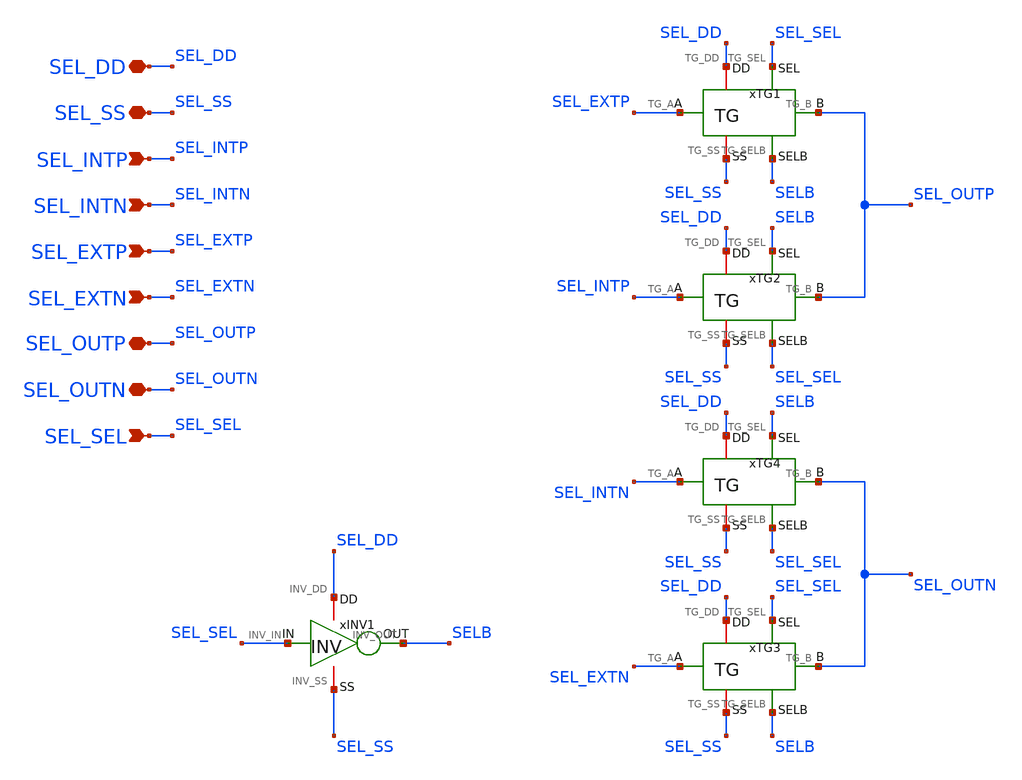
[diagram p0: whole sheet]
** sch_path: Design_Files/IC Design/Schematic/AFE_BLOCKS/SEL/SEL.sch
**.subckt SEL SEL_DD SEL_SS SEL_INTP SEL_INTN SEL_OUTP SEL_OUTN SEL_EXTP SEL_EXTN SEL_SEL
*.iopin SEL_DD
*.iopin SEL_SS
*.ipin SEL_INTP
*.ipin SEL_INTN
*.iopin SEL_OUTP
*.iopin SEL_OUTN
*.ipin SEL_EXTP
*.ipin SEL_EXTN
*.ipin SEL_SEL
xINV1 SEL_DD SEL_SS SEL_SEL SELB INV
xTG1 SEL_DD SEL_SS SEL_EXTP SEL_OUTP SEL_SEL SELB TG
xTG2 SEL_DD SEL_SS SEL_INTP SEL_OUTP SELB SEL_SEL TG
xTG3 SEL_DD SEL_SS SEL_EXTN SEL_OUTN SEL_SEL SELB TG
xTG4 SEL_DD SEL_SS SEL_INTN SEL_OUTN SELB SEL_SEL TG
**.ends

* expanding   symbol:  ECG_Acquisition_IC/Design_Files/IC Design/Schematic/AFE_BLOCKS/INV/INV.sym #
*+ of pins=4
** sym_path: Design_Files/IC Design/Schematic/INV/INV.sym
** sch_path: Design_Files/IC Design/Schematic/INV/INV.sch
.subckt INV INV_DD INV_SS INV_IN INV_OUT
*.iopin INV_DD
*.iopin INV_SS
*.ipin INV_IN
*.opin INV_OUT
XMINVP INV_OUT INV_IN INV_DD INV_DD pfet_03v3 L=0.5u W=2u nf=1 ad='int((nf+1)/2) * W/nf * 0.18u' as='int((nf+2)/2) * W/nf * 0.18u'
+ pd='2*int((nf+1)/2) * (W/nf + 0.18u)' ps='2*int((nf+2)/2) * (W/nf + 0.18u)' nrd='0.18u / W' nrs='0.18u / W'
+ sa=0 sb=0 sd=0 m=1
XMINVN INV_OUT INV_IN INV_SS INV_SS nfet_03v3 L=0.5u W=1u nf=1 ad='int((nf+1)/2) * W/nf * 0.18u' as='int((nf+2)/2) * W/nf * 0.18u'
+ pd='2*int((nf+1)/2) * (W/nf + 0.18u)' ps='2*int((nf+2)/2) * (W/nf + 0.18u)' nrd='0.18u / W' nrs='0.18u / W'
+ sa=0 sb=0 sd=0 m=1
.ends


* expanding   symbol:  ECG_Acquisition_IC/Design_Files/IC Design/Schematic/AFE_BLOCKS/TG/TG.sym # of
*+ pins=6
** sym_path: Design_Files/IC Design/Schematic/TG/TG.sym
** sch_path: Design_Files/IC Design/Schematic/TG/TG.sch
.subckt TG TG_DD TG_SS TG_A TG_B TG_SEL TG_SELB
*.iopin TG_DD
*.iopin TG_SS
*.iopin TG_A
*.iopin TG_B
*.ipin TG_SEL
*.ipin TG_SELB
XMTGP TG_B TG_SELB TG_A TG_DD pfet_03v3 L=0.5u W=40u nf=1 ad='int((nf+1)/2) * W/nf * 0.18u' as='int((nf+2)/2) * W/nf * 0.18u'
+ pd='2*int((nf+1)/2) * (W/nf + 0.18u)' ps='2*int((nf+2)/2) * (W/nf + 0.18u)' nrd='0.18u / W' nrs='0.18u / W'
+ sa=0 sb=0 sd=0 m=1
XMTGN TG_A TG_SEL TG_B TG_SS nfet_03v3 L=0.5u W=20u nf=1 ad='int((nf+1)/2) * W/nf * 0.18u' as='int((nf+2)/2) * W/nf * 0.18u'
+ pd='2*int((nf+1)/2) * (W/nf + 0.18u)' ps='2*int((nf+2)/2) * (W/nf + 0.18u)' nrd='0.18u / W' nrs='0.18u / W'
+ sa=0 sb=0 sd=0 m=1
.ends

.end
